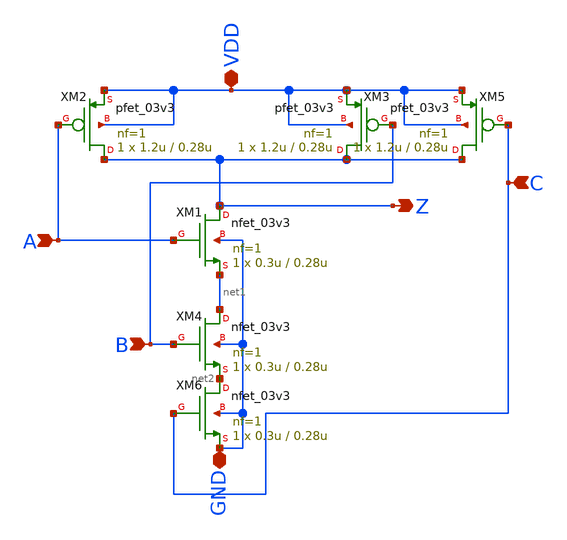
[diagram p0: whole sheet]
** sch_path: rha-vga-pll-blocks/blocks/pll/nand3.sch
**.subckt nand3 A VDD Z GND B C
*.ipin A
*.iopin VDD
*.opin Z
*.iopin GND
*.ipin B
*.ipin C
XM1 Z A net1 GND nfet_03v3 L=0.28u W=0.3u nf=1 ad='int((nf+1)/2) * W/nf * 0.18u' as='int((nf+2)/2) * W/nf * 0.18u'
+ pd='2*int((nf+1)/2) * (W/nf + 0.18u)' ps='2*int((nf+2)/2) * (W/nf + 0.18u)' nrd='0.18u / W' nrs='0.18u / W'
+ sa=0 sb=0 sd=0 m=1
XM2 Z A VDD VDD pfet_03v3 L=0.28u W=1.2u nf=1 ad='int((nf+1)/2) * W/nf * 0.18u' as='int((nf+2)/2) * W/nf * 0.18u'
+ pd='2*int((nf+1)/2) * (W/nf + 0.18u)' ps='2*int((nf+2)/2) * (W/nf + 0.18u)' nrd='0.18u / W' nrs='0.18u / W'
+ sa=0 sb=0 sd=0 m=1
XM3 Z B VDD VDD pfet_03v3 L=0.28u W=1.2u nf=1 ad='int((nf+1)/2) * W/nf * 0.18u' as='int((nf+2)/2) * W/nf * 0.18u'
+ pd='2*int((nf+1)/2) * (W/nf + 0.18u)' ps='2*int((nf+2)/2) * (W/nf + 0.18u)' nrd='0.18u / W' nrs='0.18u / W'
+ sa=0 sb=0 sd=0 m=1
XM4 net1 B net2 GND nfet_03v3 L=0.28u W=0.3u nf=1 ad='int((nf+1)/2) * W/nf * 0.18u' as='int((nf+2)/2) * W/nf * 0.18u'
+ pd='2*int((nf+1)/2) * (W/nf + 0.18u)' ps='2*int((nf+2)/2) * (W/nf + 0.18u)' nrd='0.18u / W' nrs='0.18u / W'
+ sa=0 sb=0 sd=0 m=1
XM5 Z C VDD VDD pfet_03v3 L=0.28u W=1.2u nf=1 ad='int((nf+1)/2) * W/nf * 0.18u' as='int((nf+2)/2) * W/nf * 0.18u'
+ pd='2*int((nf+1)/2) * (W/nf + 0.18u)' ps='2*int((nf+2)/2) * (W/nf + 0.18u)' nrd='0.18u / W' nrs='0.18u / W'
+ sa=0 sb=0 sd=0 m=1
XM6 net2 C GND GND nfet_03v3 L=0.28u W=0.3u nf=1 ad='int((nf+1)/2) * W/nf * 0.18u' as='int((nf+2)/2) * W/nf * 0.18u'
+ pd='2*int((nf+1)/2) * (W/nf + 0.18u)' ps='2*int((nf+2)/2) * (W/nf + 0.18u)' nrd='0.18u / W' nrs='0.18u / W'
+ sa=0 sb=0 sd=0 m=1
**.ends
.end
